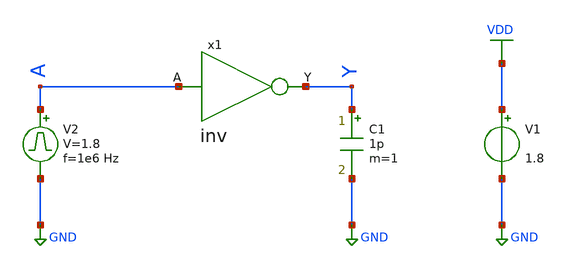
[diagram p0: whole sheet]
** sch_path: library/xschem/inv_tb.sch
**.subckt inv_tb
V1 VDD GND 1.8
V2 A GND pulse 0 1.8 '0.495/ 1e6 ' '0.01/1e6 ' '0.01/1e6 ' '0.49/1e6 ' '1/1e6 '
C1 Y GND 1p m=1
x1 A Y inv
**** begin user architecture code


.control
save all
tran 1n 2u
plot V(A) V(Y)
.endc


** opencircuitdesign pdks install
.lib $::SKYWATER_MODELS/sky130.lib.spice tt


**** end user architecture code
**.ends

* expanding   symbol:  inv.sym # of pins=2
** sym_path: library/xschem/inv.sym
** sch_path: library/xschem/inv.sch
.subckt inv A Y
*.opin Y
*.ipin A
XM1 Y A GND GND sky130_fd_pr__nfet_01v8 L=0.15 W=1 nf=1 ad='int((nf+1)/2) * W/nf * 0.29' as='int((nf+2)/2) * W/nf * 0.29'
+ pd='2*int((nf+1)/2) * (W/nf + 0.29)' ps='2*int((nf+2)/2) * (W/nf + 0.29)' nrd='0.29 / W' nrs='0.29 / W'
+ sa=0 sb=0 sd=0 mult=1 m=1
XM2 Y A VDD VDD sky130_fd_pr__pfet_01v8 L=0.15 W=1 nf=1 ad='int((nf+1)/2) * W/nf * 0.29' as='int((nf+2)/2) * W/nf * 0.29'
+ pd='2*int((nf+1)/2) * (W/nf + 0.29)' ps='2*int((nf+2)/2) * (W/nf + 0.29)' nrd='0.29 / W' nrs='0.29 / W'
+ sa=0 sb=0 sd=0 mult=1 m=1
.ends

.GLOBAL VDD
.GLOBAL GND
.end
